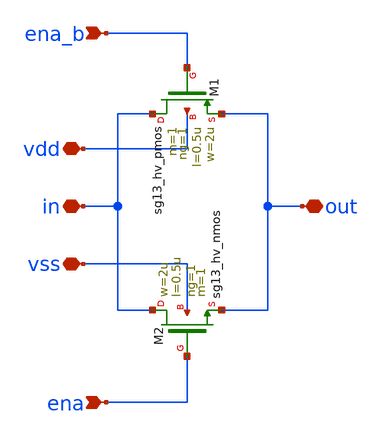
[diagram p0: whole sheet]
** sch_path: macros/ocd_analog_switches/schematic/xschem/xgate.sch
**.subckt xgate out in vdd vss ena_b ena
*.iopin out
*.iopin in
*.iopin vdd
*.iopin vss
*.ipin ena_b
*.ipin ena
XM1 in ena_b out vdd sg13_hv_pmos w=2u l=0.5u ng=1 m=1 mm_ok=1
XM2 in ena out vss sg13_hv_nmos w=2u l=0.5u ng=1 m=1 mm_ok=1
**.ends
.end
